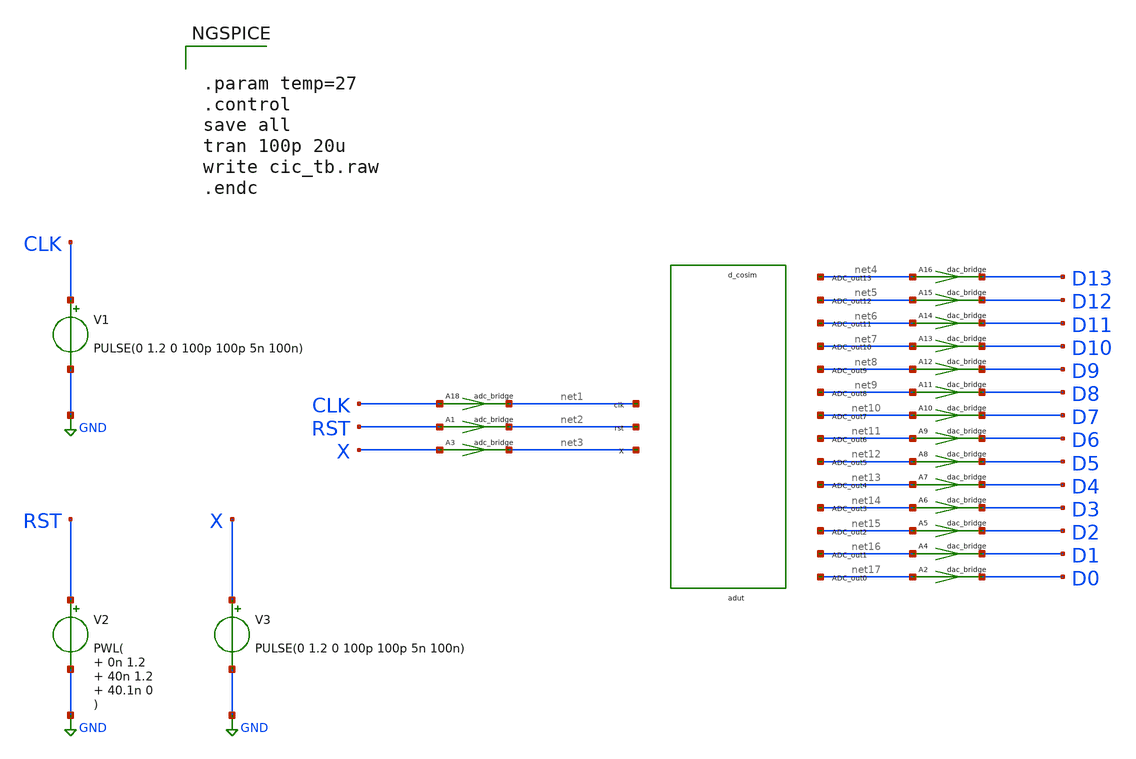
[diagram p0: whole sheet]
** sch_path: xschem/cic_tb.sch
**.subckt cic_tb
V1 CLK GND PULSE(0 1.2 0 100p 100p 5n 100n)
V2 RST GND PWL( 0n 1.2 40n 1.2 40.1n 0
)
V3 X GND PULSE(0 1.2 0 100p 100p 5n 100n)
A18 [ CLK ] [ net1 ] adc1
.model adc1 adc_bridge in_low=0.1 in_high=0.9
A1 [ RST ] [ net2 ] adc1
.model adc1 adc_bridge in_low=0.1 in_high=0.9
A3 [ X ] [ net3 ] adc1
.model adc1 adc_bridge in_low=0.1 in_high=0.9
A2 [ net17 ] [ D0 ] dac1
.model dac1 dac_bridge out_low=0 out_high=1.2
A4 [ net16 ] [ D1 ] dac1
.model dac1 dac_bridge out_low=0 out_high=1.2
A5 [ net15 ] [ D2 ] dac1
.model dac1 dac_bridge out_low=0 out_high=1.2
A6 [ net14 ] [ D3 ] dac1
.model dac1 dac_bridge out_low=0 out_high=1.2
A7 [ net13 ] [ D4 ] dac1
.model dac1 dac_bridge out_low=0 out_high=1.2
A8 [ net12 ] [ D5 ] dac1
.model dac1 dac_bridge out_low=0 out_high=1.2
A9 [ net11 ] [ D6 ] dac1
.model dac1 dac_bridge out_low=0 out_high=1.2
A10 [ net10 ] [ D7 ] dac1
.model dac1 dac_bridge out_low=0 out_high=1.2
A11 [ net9 ] [ D8 ] dac1
.model dac1 dac_bridge out_low=0 out_high=1.2
A12 [ net8 ] [ D9 ] dac1
.model dac1 dac_bridge out_low=0 out_high=1.2
A13 [ net7 ] [ D10 ] dac1
.model dac1 dac_bridge out_low=0 out_high=1.2
A14 [ net6 ] [ D11 ] dac1
.model dac1 dac_bridge out_low=0 out_high=1.2
A15 [ net5 ] [ D12 ] dac1
.model dac1 dac_bridge out_low=0 out_high=1.2
A16 [ net4 ] [ D13 ] dac1
.model dac1 dac_bridge out_low=0 out_high=1.2
adut [ net1 net2 net3 ] [ net4 net5 net6 net7 net8 net9 net10 net11 net12 net13 net14 net15 net16
+ net17 ] null dut
.model dut d_cosim simulation=./CIC_wrapper.so
**** begin user architecture code


.param temp=27
.control
save all
tran 100p 20u
write cic_tb.raw
.endc


**** end user architecture code
**.ends
.GLOBAL GND
.end
